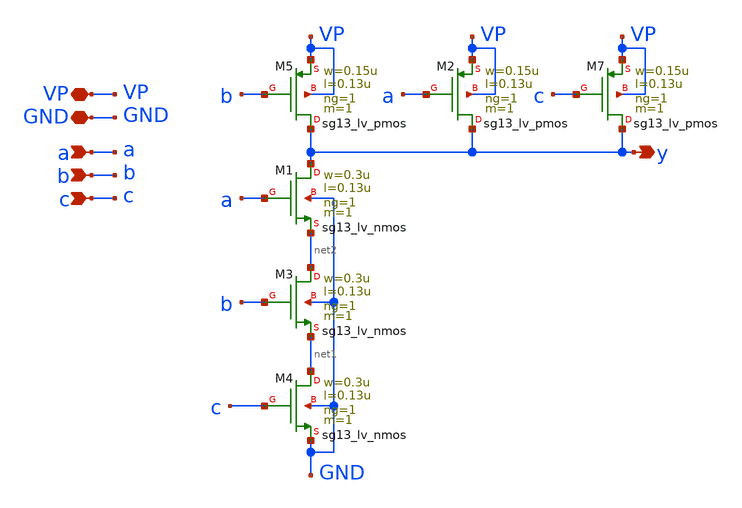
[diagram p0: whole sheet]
** sch_path: PLL0663-main/schematic/xschem/divider/NAND_3in.sch
**.subckt NAND_3in y GND a VP b c
*.opin y
*.iopin GND
*.ipin a
*.iopin VP
*.ipin b
*.ipin c
XM1 y a net2 GND sg13_lv_nmos w=0.3u l=0.13u ng=1 m=1 mm_ok=1
XM3 net2 b net1 GND sg13_lv_nmos w=0.3u l=0.13u ng=1 m=1 mm_ok=1
XM4 net1 c GND GND sg13_lv_nmos w=0.3u l=0.13u ng=1 m=1 mm_ok=1
XM7 y c VP VP sg13_lv_pmos w=0.15u l=0.13u ng=1 m=1 mm_ok=1
XM2 y a VP VP sg13_lv_pmos w=0.15u l=0.13u ng=1 m=1 mm_ok=1
XM5 y b VP VP sg13_lv_pmos w=0.15u l=0.13u ng=1 m=1 mm_ok=1
**.ends
.end
